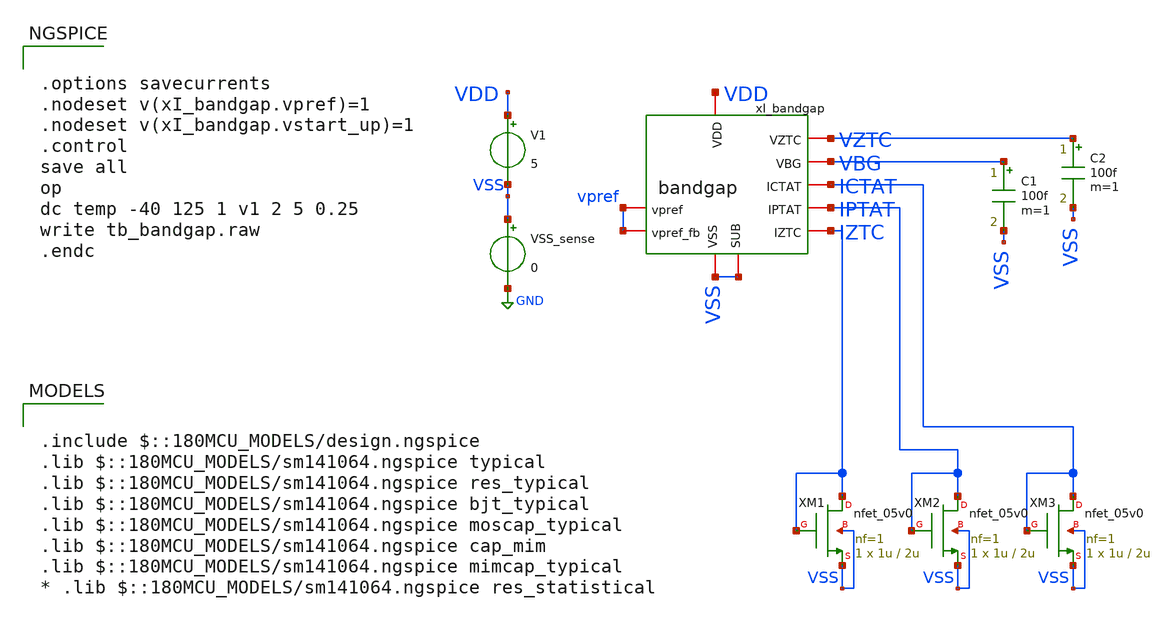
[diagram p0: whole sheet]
** sch_path: designs/libs/tb_bandgap/tb_bandgap/tb_bandgap.sch
**.subckt tb_bandgap
V1 VDD VSS 5
VSS_sense VSS GND 0
C1 VBG VSS 100f m=1
xI_bandgap VDD VBG IPTAT IZTC VSS VSS vpref vpref ICTAT VZTC bandgap
C2 VZTC VSS 100f m=1
XM1 IZTC IZTC VSS VSS nfet_05v0 L=2u W=1u nf=1 ad='int((nf+1)/2) * W/nf * 0.18u' as='int((nf+2)/2) * W/nf * 0.18u'
+ pd='2*int((nf+1)/2) * (W/nf + 0.18u)' ps='2*int((nf+2)/2) * (W/nf + 0.18u)' nrd='0.18u / W' nrs='0.18u / W'
+ sa=0 sb=0 sd=0 m=1
XM2 IPTAT IPTAT VSS VSS nfet_05v0 L=2u W=1u nf=1 ad='int((nf+1)/2) * W/nf * 0.18u' as='int((nf+2)/2) * W/nf * 0.18u'
+ pd='2*int((nf+1)/2) * (W/nf + 0.18u)' ps='2*int((nf+2)/2) * (W/nf + 0.18u)' nrd='0.18u / W' nrs='0.18u / W'
+ sa=0 sb=0 sd=0 m=1
XM3 ICTAT ICTAT VSS VSS nfet_05v0 L=2u W=1u nf=1 ad='int((nf+1)/2) * W/nf * 0.18u' as='int((nf+2)/2) * W/nf * 0.18u'
+ pd='2*int((nf+1)/2) * (W/nf + 0.18u)' ps='2*int((nf+2)/2) * (W/nf + 0.18u)' nrd='0.18u / W' nrs='0.18u / W'
+ sa=0 sb=0 sd=0 m=1
**** begin user architecture code

.include $::180MCU_MODELS/design.ngspice
.lib $::180MCU_MODELS/sm141064.ngspice typical
.lib $::180MCU_MODELS/sm141064.ngspice res_typical
.lib $::180MCU_MODELS/sm141064.ngspice bjt_typical
.lib $::180MCU_MODELS/sm141064.ngspice moscap_typical
.lib $::180MCU_MODELS/sm141064.ngspice cap_mim
.lib $::180MCU_MODELS/sm141064.ngspice mimcap_typical
* .lib $::180MCU_MODELS/sm141064.ngspice res_statistical



.options savecurrents
.nodeset v(xI_bandgap.vpref)=1
.nodeset v(xI_bandgap.vstart_up)=1
.control
save all
op
dc temp -40 125 1 v1 2 5 0.25
write tb_bandgap.raw
.endc


**** end user architecture code
**.ends
.GLOBAL GND
.end
